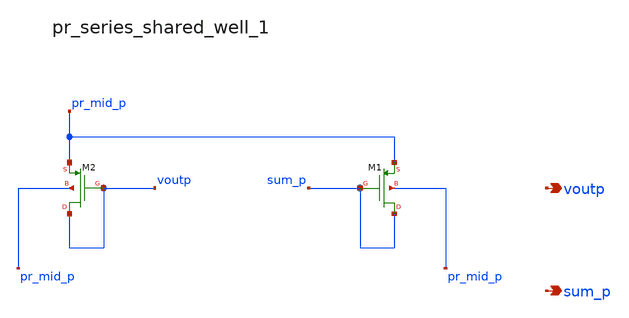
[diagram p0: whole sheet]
** sch_path: analog-db/raw/ia_001_hsu_bandpass_classab/hier/blocks/pr_series_shared_well_1.sch
**.subckt pr_series_shared_well_1 voutp sum_p
*.opin voutp
*.opin sum_p
XM1 sum_p sum_p pr_mid_p pr_mid_p sg13_lv_pmos w=x_dut_xm1_w l=x_dut_xm1_l ng=1 m=x_dut_xm1_m
XM2 voutp voutp pr_mid_p pr_mid_p sg13_lv_pmos w=x_dut_xm2_w l=x_dut_xm2_l ng=1 m=x_dut_xm2_m
**.ends
.end
